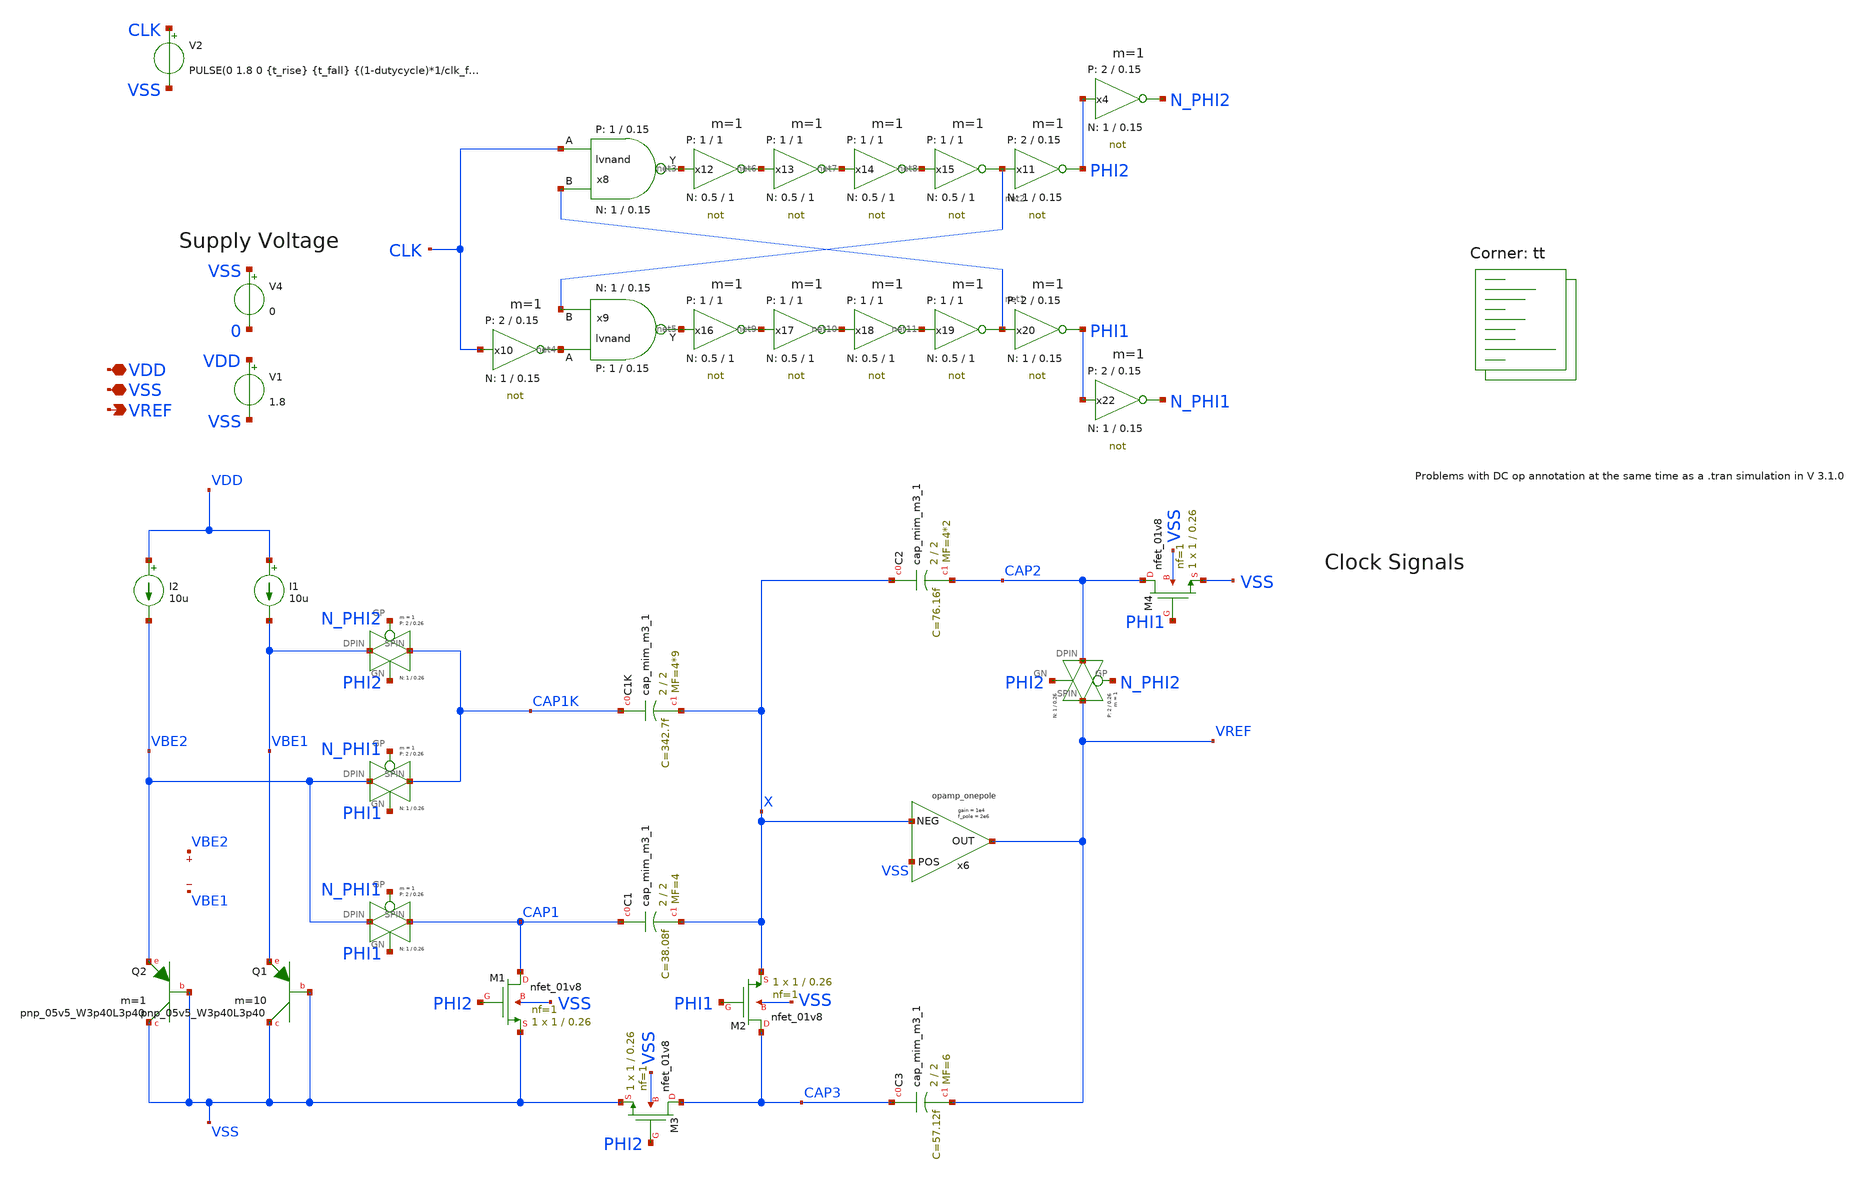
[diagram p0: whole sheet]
** sch_path: sc_bandgap.sch
* StefanSchippers/xschem_sky130/sky130_tests/lvnand.sch:
* Copyright 2021 Stefan Frederik Schippers
* Licensed under the Apache License, Version 2.0 (the "License");
**.subckt sc_bandgap VDD VREF VSS
*.iopin VDD
*.opin VREF
*.iopin VSS
I2 VDD VBE2 10u
I1 VDD VBE1 10u
XQ1 VSS VSS VBE1 sky130_fd_pr__pnp_05v5_W3p40L3p40 m=10
XQ2 VSS VSS VBE2 sky130_fd_pr__pnp_05v5_W3p40L3p40 m=1
V1 VDD VSS 1.8
V2 CLK VSS PULSE(0 1.8 0 {t_rise} {t_fall} {(1-dutycycle)*1/clk_freq} {1/clk_freq} 0)
V4 VSS 0 0
XC1K CAP1K X sky130_fd_pr__cap_mim_m3_1 W=2 L=2 MF=4*9 m=4*9
XC1 CAP1 X sky130_fd_pr__cap_mim_m3_1 W=2 L=2 MF=4 m=4
XC3 CAP3 VREF sky130_fd_pr__cap_mim_m3_1 W=2 L=2 MF=6 m=6
XC2 X CAP2 sky130_fd_pr__cap_mim_m3_1 W=2 L=2 MF=4*2 m=4*2
XM1 CAP1 PHI2 VSS VSS sky130_fd_pr__nfet_01v8 L=0.26 W=1 nf=1 ad='int((nf+1)/2) * W/nf * 0.29' as='int((nf+2)/2) * W/nf * 0.29'
+ pd='2*int((nf+1)/2) * (W/nf + 0.29)' ps='2*int((nf+2)/2) * (W/nf + 0.29)' nrd='0.29 / W' nrs='0.29 / W'
+ sa=0 sb=0 sd=0 mult=1 m=1
XM2 CAP3 PHI1 X VSS sky130_fd_pr__nfet_01v8 L=0.26 W=1 nf=1 ad='int((nf+1)/2) * W/nf * 0.29' as='int((nf+2)/2) * W/nf * 0.29'
+ pd='2*int((nf+1)/2) * (W/nf + 0.29)' ps='2*int((nf+2)/2) * (W/nf + 0.29)' nrd='0.29 / W' nrs='0.29 / W'
+ sa=0 sb=0 sd=0 mult=1 m=1
XM3 CAP3 PHI2 VSS VSS sky130_fd_pr__nfet_01v8 L=0.26 W=1 nf=1 ad='int((nf+1)/2) * W/nf * 0.29' as='int((nf+2)/2) * W/nf * 0.29'
+ pd='2*int((nf+1)/2) * (W/nf + 0.29)' ps='2*int((nf+2)/2) * (W/nf + 0.29)' nrd='0.29 / W' nrs='0.29 / W'
+ sa=0 sb=0 sd=0 mult=1 m=1
XM4 CAP2 PHI1 VSS VSS sky130_fd_pr__nfet_01v8 L=0.26 W=1 nf=1 ad='int((nf+1)/2) * W/nf * 0.29' as='int((nf+2)/2) * W/nf * 0.29'
+ pd='2*int((nf+1)/2) * (W/nf + 0.29)' ps='2*int((nf+2)/2) * (W/nf + 0.29)' nrd='0.29 / W' nrs='0.29 / W'
+ sa=0 sb=0 sd=0 mult=1 m=1
x1 N_PHI2 VBE1 CAP1K PHI2 VDD VSS transmissiongate W_P=2 L_P=0.26 W_N=1 L_N=0.26 m=1
x2 N_PHI1 VBE2 CAP1K PHI1 VDD VSS transmissiongate W_P=2 L_P=0.26 W_N=1 L_N=0.26 m=1
x3 N_PHI1 VBE2 CAP1 PHI1 VDD VSS transmissiongate W_P=2 L_P=0.26 W_N=1 L_N=0.26 m=1
.save v(vbe2)
.save v(vbe1)
x8 CLK net1 net3 VDD VSS lvnand WidthN=1 LenN=0.15 WidthP=1 LenP=0.15 m=1
x9 net4 net2 net5 VDD VSS lvnand WidthN=1 LenN=0.15 WidthP=1 LenP=0.15 m=1
x10 net4 CLK VDD VSS not W_N=1 L_N=0.15 W_P=2 L_P=0.15 m=1
x11 PHI2 net2 VDD VSS not W_N=1 L_N=0.15 W_P=2 L_P=0.15 m=1
x12 net6 net3 VDD VSS not W_N=0.5 L_N=1 W_P=1 L_P=1 m=1
x13 net7 net6 VDD VSS not W_N=0.5 L_N=1 W_P=1 L_P=1 m=1
x14 net8 net7 VDD VSS not W_N=0.5 L_N=1 W_P=1 L_P=1 m=1
x15 net2 net8 VDD VSS not W_N=0.5 L_N=1 W_P=1 L_P=1 m=1
x16 net9 net5 VDD VSS not W_N=0.5 L_N=1 W_P=1 L_P=1 m=1
x17 net10 net9 VDD VSS not W_N=0.5 L_N=1 W_P=1 L_P=1 m=1
x18 net11 net10 VDD VSS not W_N=0.5 L_N=1 W_P=1 L_P=1 m=1
x19 net1 net11 VDD VSS not W_N=0.5 L_N=1 W_P=1 L_P=1 m=1
x20 PHI1 net1 VDD VSS not W_N=1 L_N=0.15 W_P=2 L_P=0.15 m=1
x22 N_PHI1 PHI1 VDD VSS not W_N=1 L_N=0.15 W_P=2 L_P=0.15 m=1
x4 N_PHI2 PHI2 VDD VSS not W_N=1 L_N=0.15 W_P=2 L_P=0.15 m=1
x5 N_PHI2 CAP2 VREF PHI2 VDD VSS transmissiongate W_P=2 L_P=0.26 W_N=1 L_N=0.26 m=1
x6 VSS VREF X VDD VSS opamp_onepole gain=1e4 f3db=2e6
**** begin user architecture code
.lib $::SKYWATER_MODELS/sky130.lib.spice tt



* Parameters *
.param clk_freq = 1Meg
.param dutycycle = 0.5
.param t_rise = 1n
.param t_fall = 1n

* Switch model *
.model SWITCH1 sw vt=1 vh=0.2 ron=1k roff=1Meg

* Options *
.options wnflag=1 RELTOL=0.001
*.options wnflag=1 METHOD=GEAR ITL4=100 CHGTOL=1e-15 TRTOL=1 RELTOL=0.0001 VNTOL=0.1u
.options savecurrents
.save all
.save @m.xm1.msky130_fd_pr__nfet_01v8[gds]
.save @m.xm1.msky130_fd_pr__nfet_01v8[gm]
.save @m.xm2.msky130_fd_pr__nfet_01v8[gds]
.save @q.xq1.qsky130_fd_pr__pnp_05v5_W3p40L3p40[p]

* Control *
.control
let run = 1
set temp=0
while run <= 2
   if run > 1
      reset
      set appendwrite
   end
   let dtemp = 0 + 80*(run-1)
   set temp=$&dtemp
   tran 1n 10u 8u
   write sc_bandgap.raw
   let run = run + 1
end
reset
op
set appendwrite
write sc_bandgap.raw
.endc






**** end user architecture code
**.ends

* expanding   symbol:  transmissiongate.sym # of pins=4
** sym_path: transmissiongate.sym
** sch_path: transmissiongate.sch
.subckt transmissiongate GP DPIN SPIN GN VDDBPIN VSSBPIN  W_P=1 L_P=0.2 W_N=1 L_N=0.2
*.iopin DPIN
*.iopin SPIN
*.ipin GP
*.ipin GN
XM1 DPIN GN SPIN VSSBPIN sky130_fd_pr__nfet_01v8 L=L_N W=W_N nf=1 ad='int((nf+1)/2) * W/nf * 0.29' as='int((nf+2)/2) * W/nf * 0.29'
+ pd='2*int((nf+1)/2) * (W/nf + 0.29)' ps='2*int((nf+2)/2) * (W/nf + 0.29)' nrd='0.29 / W' nrs='0.29 / W'
+ sa=0 sb=0 sd=0 mult=1 m=1
XM2 DPIN GP SPIN VDDBPIN sky130_fd_pr__pfet_01v8 L=L_P W=W_P nf=1 ad='int((nf+1)/2) * W/nf * 0.29' as='int((nf+2)/2) * W/nf * 0.29'
+ pd='2*int((nf+1)/2) * (W/nf + 0.29)' ps='2*int((nf+2)/2) * (W/nf + 0.29)' nrd='0.29 / W' nrs='0.29 / W'
+ sa=0 sb=0 sd=0 mult=1 m=1
* noconn VDDBPIN
* noconn VSSBPIN
.ends


* expanding   symbol:  sky130_tests/lvnand.sym # of pins=3
** sym_path: sky130_tests/lvnand.sym
** sch_path: sky130_tests/lvnand.sch
.subckt lvnand A B Y VCCPIN VSSPIN  WidthN=1 LenN=0.15 WidthP=1 LenP=0.15
*.ipin A
*.ipin B
*.opin Y
XM1 Y B S VSSPIN sky130_fd_pr__nfet_01v8 L=LenN W=WidthN nf=1 ad='int((nf+1)/2) * W/nf * 0.29' as='int((nf+2)/2) * W/nf * 0.29'
+ pd='2*int((nf+1)/2) * (W/nf + 0.29)' ps='2*int((nf+2)/2) * (W/nf + 0.29)' nrd='0.29 / W' nrs='0.29 / W'
+ sa=0 sb=0 sd=0 mult=1 m=1
XM2 Y A VCCPIN VCCPIN sky130_fd_pr__pfet_01v8 L=LenP W=WidthP nf=1 ad='int((nf+1)/2) * W/nf * 0.29' as='int((nf+2)/2) * W/nf * 0.29'
+ pd='2*int((nf+1)/2) * (W/nf + 0.29)' ps='2*int((nf+2)/2) * (W/nf + 0.29)' nrd='0.29 / W' nrs='0.29 / W'
+ sa=0 sb=0 sd=0 mult=1 m=1
XM3 Y B VCCPIN VCCPIN sky130_fd_pr__pfet_01v8 L=LenP W=WidthP nf=1 ad='int((nf+1)/2) * W/nf * 0.29' as='int((nf+2)/2) * W/nf * 0.29'
+ pd='2*int((nf+1)/2) * (W/nf + 0.29)' ps='2*int((nf+2)/2) * (W/nf + 0.29)' nrd='0.29 / W' nrs='0.29 / W'
+ sa=0 sb=0 sd=0 mult=1 m=1
XM4 S A VSSPIN VSSPIN sky130_fd_pr__nfet_01v8 L=LenN W=WidthN nf=1 ad='int((nf+1)/2) * W/nf * 0.29' as='int((nf+2)/2) * W/nf * 0.29'
+ pd='2*int((nf+1)/2) * (W/nf + 0.29)' ps='2*int((nf+2)/2) * (W/nf + 0.29)' nrd='0.29 / W' nrs='0.29 / W'
+ sa=0 sb=0 sd=0 mult=1 m=1
.ends


* expanding   symbol:  sky130_tests/not.sym # of pins=2
** sym_path: sky130_tests/not.sym
** sch_path: sky130_tests/not.sch
.subckt not y a VCCPIN VSSPIN     W_N=1 L_N=0.15 W_P=2 L_P=0.15
*.opin y
*.ipin a
XM1 DN a VSSPIN VSSPIN sky130_fd_pr__nfet_01v8 L=L_N W=W_N nf=1 ad='int((1 + 1)/2) * W_N / 1 * 0.29'
+ as='int((1 + 2)/2) * W_N / 1 * 0.29' pd='2*int((1 + 1)/2) * (W_N / 1 + 0.29)' ps='2*int((1 + 2)/2) * (W_N / 1 + 0.29)'
+ nrd='0.29 / W_N ' nrs='0.29 / W_N ' sa=0 sb=0 sd=0 mult=1 m=1
XM2 DP a VCCPIN VCCPIN sky130_fd_pr__pfet_01v8 L=L_P W=W_P nf=1 ad='int((nf+1)/2) * W/nf * 0.29' as='int((nf+2)/2) * W/nf * 0.29'
+ pd='2*int((nf+1)/2) * (W/nf + 0.29)' ps='2*int((nf+2)/2) * (W/nf + 0.29)' nrd='0.29 / W' nrs='0.29 / W'
+ sa=0 sb=0 sd=0 mult=1 m=1
Vmeas DP y 0
.save i(vmeas)
Vmeas1 y DN 0
.save i(vmeas1)
.save v(dp)
.save v(dn)
.ends


* expanding   symbol:  opamp_onepole.sym # of pins=3
** sym_path: opamp_onepole.sym
** sch_path: opamp_onepole.sch
.subckt opamp_onepole POS OUT NEG VDDPIN VSSPIN  gain=1e4 f3db=2e6
*.opin OUT
*.ipin POS
*.ipin NEG
E1 VDIFF VSSPIN VOL=' (V(POS)-V(NEG))*gain > V(VDDPIN) ? V(VDDPIN) : (V(POS)-V(NEG))*gain < V(VSSPIN) ? V(VSSPIN) : (V(POS)-V(NEG))*gain '
R3 SR VDIFF 1k m=1
C2 SR VSSPIN {1/(2*3.149*1e3*f3db)} m=1
E2 OUT VSSPIN VOL=' V(SR)*1 '
* noconn POS
* noconn NEG
* noconn VDDPIN
.ends

.end
